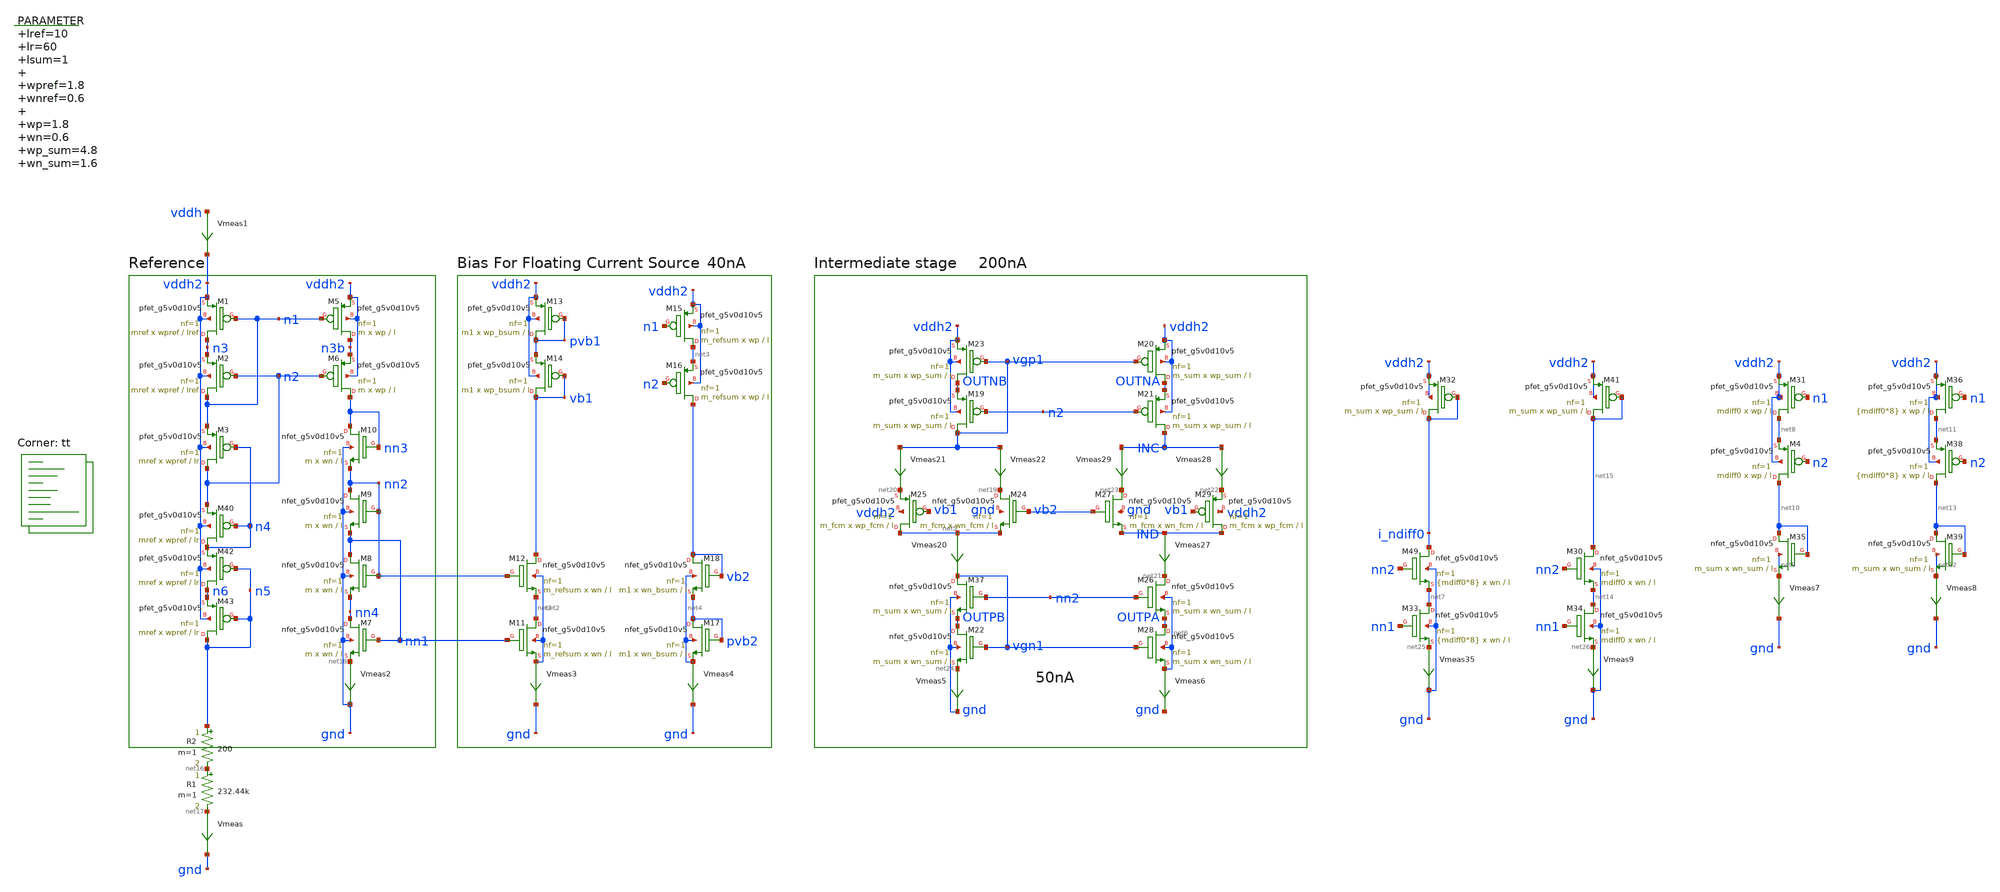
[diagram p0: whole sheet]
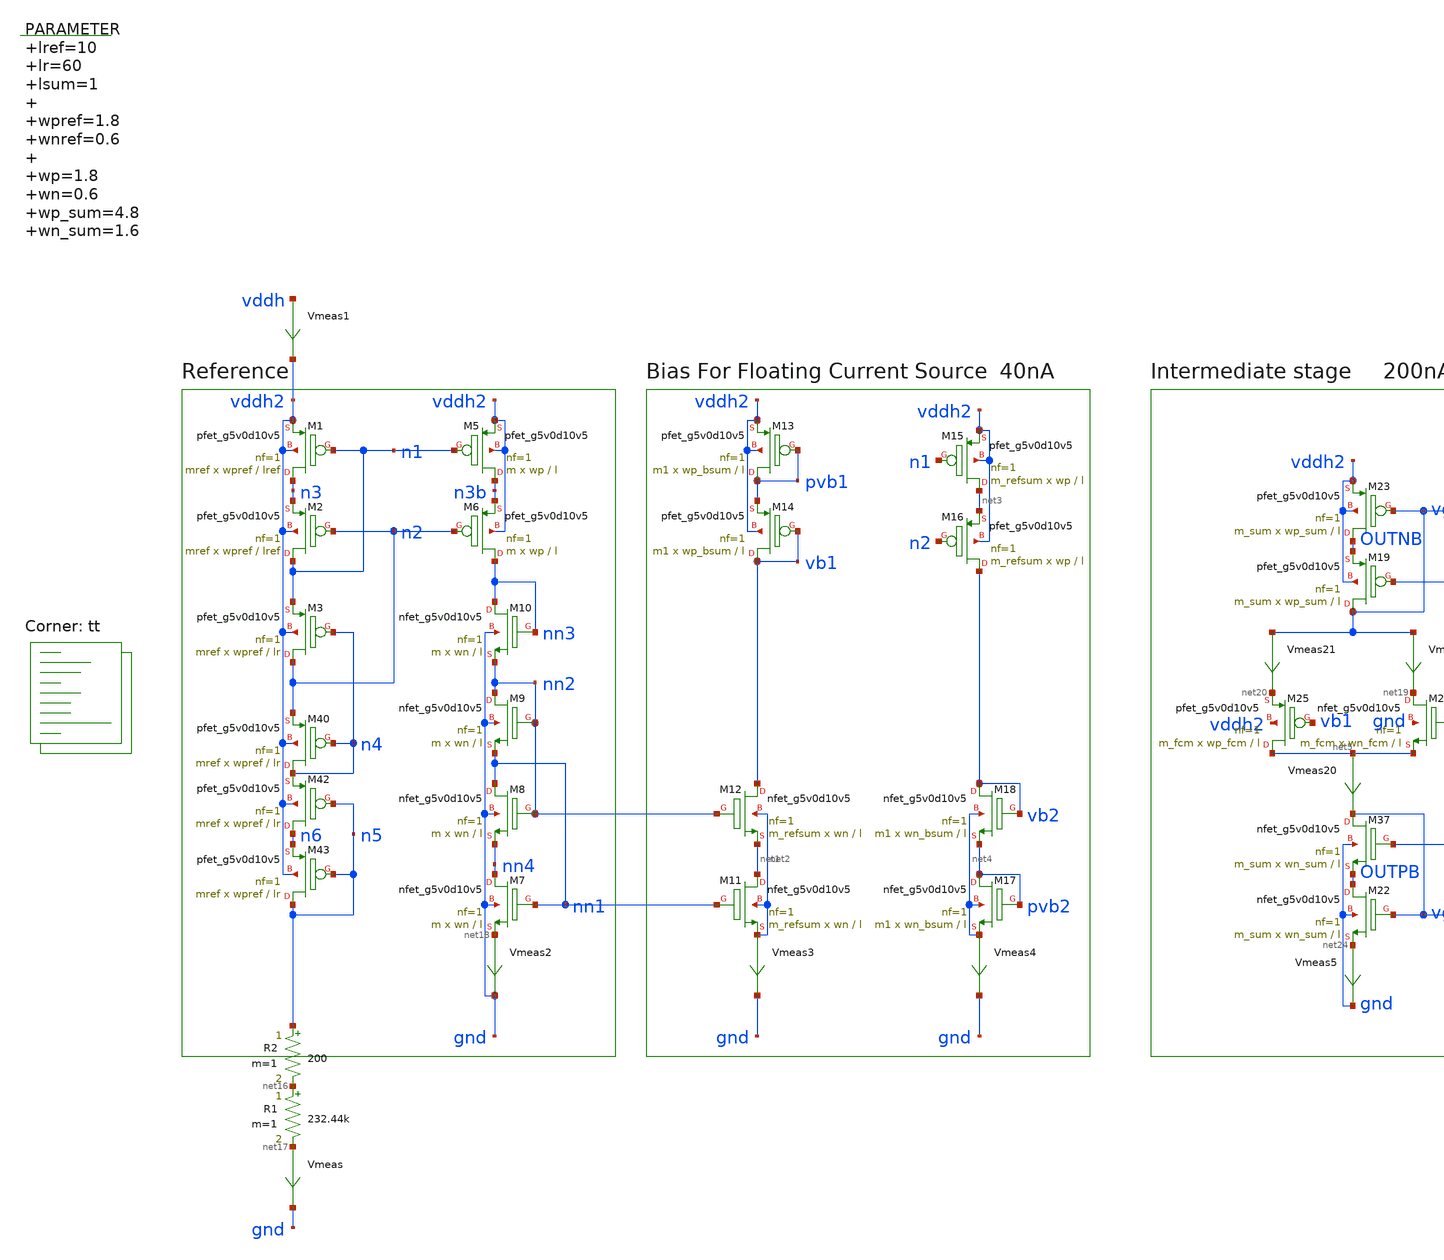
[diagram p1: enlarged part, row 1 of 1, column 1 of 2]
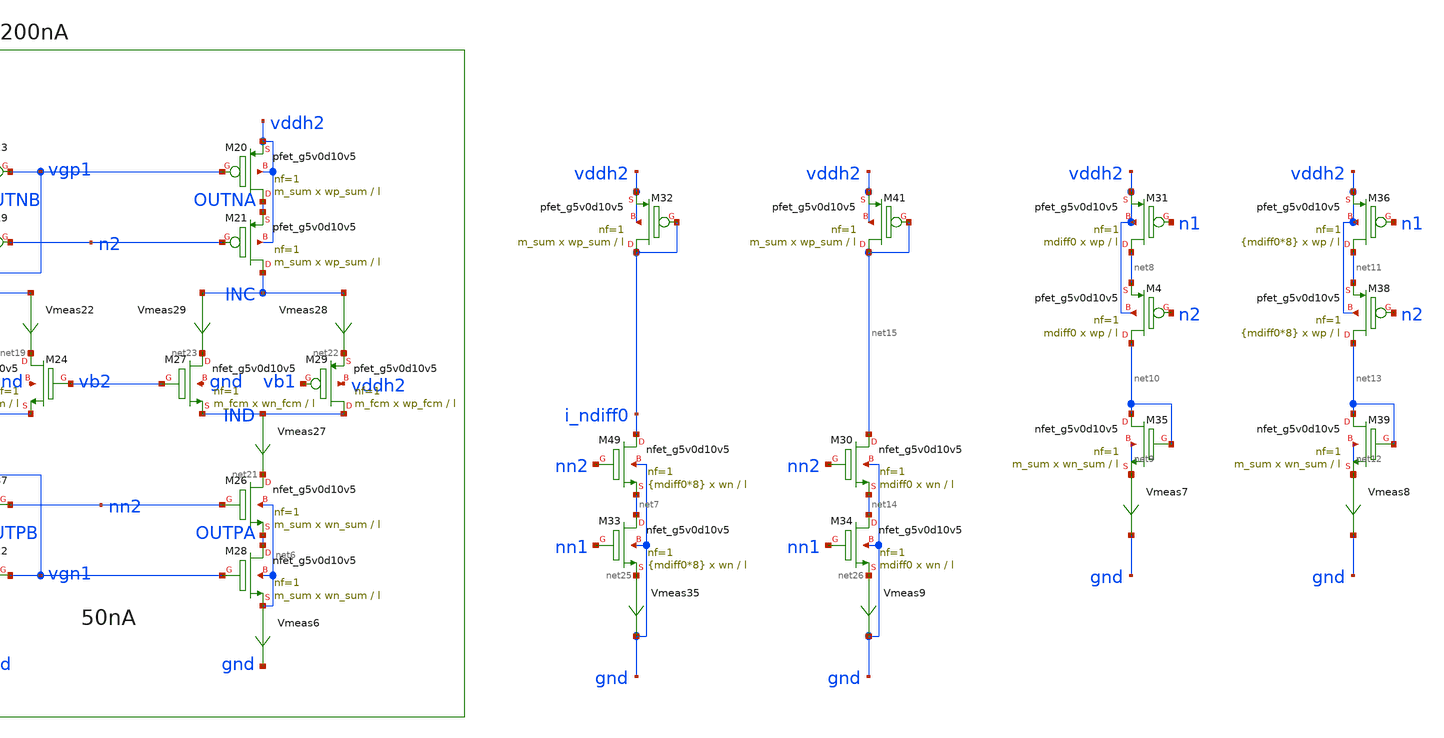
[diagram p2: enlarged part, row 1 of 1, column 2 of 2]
** sch_path: xschem/op_amp_biasing.sch
**.subckt op_amp_biasing
.param lref=10 lr=60 lsum=1 wpref=1.8 wnref=0.6 wp=1.8 wn=0.6 wp_sum=4.8 wn_sum=1.6 wp_fcm=4.8
+ wn_fcm=1.6 wp_head=3 wn_tail=1 wp_bsum=4.8 wn_bsum=1.6 mref=8 m1=2 m_sum=2 m_refsum=5 m_fcm=2 mdiff0=2
XM1 n3 n1 vddh2 vddh2 sky130_fd_pr__pfet_g5v0d10v5 L=lref W=wpref nf=1 ad='int((nf+1)/2) * W/nf * 0.29'
+ as='int((nf+2)/2) * W/nf * 0.29' pd='2*int((nf+1)/2) * (W/nf + 0.29)' ps='2*int((nf+2)/2) * (W/nf + 0.29)'
+ nrd='0.29 / W' nrs='0.29 / W' sa=0 sb=0 sd=0 mult=mref m=mref
R1 net16 net17 232.44k m=1
Vmeas net17 gnd 0
.save i(vmeas)
R2 n5 net16 200 m=1
Vmeas1 vddh vddh2 0
.save i(vmeas1)
XM7 nn4 nn1 net18 gnd sky130_fd_pr__nfet_g5v0d10v5 L=l W=wn nf=1 ad='int((nf+1)/2) * W/nf * 0.29' as='int((nf+2)/2) * W/nf * 0.29'
+ pd='2*int((nf+1)/2) * (W/nf + 0.29)' ps='2*int((nf+2)/2) * (W/nf + 0.29)' nrd='0.29 / W' nrs='0.29 / W'
+ sa=0 sb=0 sd=0 mult=m m=m
XM8 nn1 nn2 nn4 gnd sky130_fd_pr__nfet_g5v0d10v5 L=l W=wn nf=1 ad='int((nf+1)/2) * W/nf * 0.29' as='int((nf+2)/2) * W/nf * 0.29'
+ pd='2*int((nf+1)/2) * (W/nf + 0.29)' ps='2*int((nf+2)/2) * (W/nf + 0.29)' nrd='0.29 / W' nrs='0.29 / W'
+ sa=0 sb=0 sd=0 mult=m m=m
XM9 nn2 nn2 nn1 gnd sky130_fd_pr__nfet_g5v0d10v5 L=l W=wn nf=1 ad='int((nf+1)/2) * W/nf * 0.29' as='int((nf+2)/2) * W/nf * 0.29'
+ pd='2*int((nf+1)/2) * (W/nf + 0.29)' ps='2*int((nf+2)/2) * (W/nf + 0.29)' nrd='0.29 / W' nrs='0.29 / W'
+ sa=0 sb=0 sd=0 mult=m m=m
XM10 nn3 nn3 nn2 gnd sky130_fd_pr__nfet_g5v0d10v5 L=l W=wn nf=1 ad='int((nf+1)/2) * W/nf * 0.29' as='int((nf+2)/2) * W/nf * 0.29'
+ pd='2*int((nf+1)/2) * (W/nf + 0.29)' ps='2*int((nf+2)/2) * (W/nf + 0.29)' nrd='0.29 / W' nrs='0.29 / W'
+ sa=0 sb=0 sd=0 mult=m m=m
Vmeas2 net18 gnd 0
.save i(vmeas2)
XM5 n3b n1 vddh2 vddh2 sky130_fd_pr__pfet_g5v0d10v5 L=l W=wp nf=1 ad='int((nf+1)/2) * W/nf * 0.29' as='int((nf+2)/2) * W/nf * 0.29'
+ pd='2*int((nf+1)/2) * (W/nf + 0.29)' ps='2*int((nf+2)/2) * (W/nf + 0.29)' nrd='0.29 / W' nrs='0.29 / W'
+ sa=0 sb=0 sd=0 mult=m m=m
XM6 nn3 n2 n3b vddh2 sky130_fd_pr__pfet_g5v0d10v5 L=l W=wp nf=1 ad='int((nf+1)/2) * W/nf * 0.29' as='int((nf+2)/2) * W/nf * 0.29'
+ pd='2*int((nf+1)/2) * (W/nf + 0.29)' ps='2*int((nf+2)/2) * (W/nf + 0.29)' nrd='0.29 / W' nrs='0.29 / W'
+ sa=0 sb=0 sd=0 mult=m m=m
XM11 net1 nn1 net2 net2 sky130_fd_pr__nfet_g5v0d10v5 L=l W=wn nf=1 ad='int((nf+1)/2) * W/nf * 0.29' as='int((nf+2)/2) * W/nf * 0.29'
+ pd='2*int((nf+1)/2) * (W/nf + 0.29)' ps='2*int((nf+2)/2) * (W/nf + 0.29)' nrd='0.29 / W' nrs='0.29 / W'
+ sa=0 sb=0 sd=0 mult=m_refsum m=m_refsum
Vmeas3 net2 gnd 0
.save i(vmeas3)
XM17 pvb2 pvb2 net4 net4 sky130_fd_pr__nfet_g5v0d10v5 L=l W=wn_bsum nf=1 ad='int((nf+1)/2) * W/nf * 0.29'
+ as='int((nf+2)/2) * W/nf * 0.29' pd='2*int((nf+1)/2) * (W/nf + 0.29)' ps='2*int((nf+2)/2) * (W/nf + 0.29)'
+ nrd='0.29 / W' nrs='0.29 / W' sa=0 sb=0 sd=0 mult=m1 m=m1
XM18 vb2 vb2 pvb2 net4 sky130_fd_pr__nfet_g5v0d10v5 L=l W=wn_bsum nf=1 ad='int((nf+1)/2) * W/nf * 0.29'
+ as='int((nf+2)/2) * W/nf * 0.29' pd='2*int((nf+1)/2) * (W/nf + 0.29)' ps='2*int((nf+2)/2) * (W/nf + 0.29)'
+ nrd='0.29 / W' nrs='0.29 / W' sa=0 sb=0 sd=0 mult=m1 m=m1
Vmeas4 net4 gnd 0
.save i(vmeas4)
Vmeas20 net5 vgn1 0
.save i(vmeas20)
XM23 OUTNB vgp1 vddh2 vddh2 sky130_fd_pr__pfet_g5v0d10v5 L=l W=wp_sum nf=1 ad='int((nf+1)/2) * W/nf * 0.29'
+ as='int((nf+2)/2) * W/nf * 0.29' pd='2*int((nf+1)/2) * (W/nf + 0.29)' ps='2*int((nf+2)/2) * (W/nf + 0.29)'
+ nrd='0.29 / W' nrs='0.29 / W' sa=0 sb=0 sd=0 mult=m_sum m=m_sum
XM24 net19 vb2 net5 gnd sky130_fd_pr__nfet_g5v0d10v5 L=l W=wn_fcm nf=1 ad='int((nf+1)/2) * W/nf * 0.29'
+ as='int((nf+2)/2) * W/nf * 0.29' pd='2*int((nf+1)/2) * (W/nf + 0.29)' ps='2*int((nf+2)/2) * (W/nf + 0.29)'
+ nrd='0.29 / W' nrs='0.29 / W' sa=0 sb=0 sd=0 mult=m_fcm m=m_fcm
Vmeas21 vgp1 net20 0
.save i(vmeas21)
Vmeas22 vgp1 net19 0
.save i(vmeas22)
XM25 net5 vb1 net20 vddh2 sky130_fd_pr__pfet_g5v0d10v5 L=l W=wp_fcm nf=1 ad='int((nf+1)/2) * W/nf * 0.29'
+ as='int((nf+2)/2) * W/nf * 0.29' pd='2*int((nf+1)/2) * (W/nf + 0.29)' ps='2*int((nf+2)/2) * (W/nf + 0.29)'
+ nrd='0.29 / W' nrs='0.29 / W' sa=0 sb=0 sd=0 mult=m_fcm m=m_fcm
Vmeas27 IND net21 0
.save i(vmeas27)
Vmeas28 INC net22 0
.save i(vmeas28)
Vmeas29 INC net23 0
.save i(vmeas29)
XM37 vgn1 nn2 OUTPB gnd sky130_fd_pr__nfet_g5v0d10v5 L=l W=wn_sum nf=1 ad='int((nf+1)/2) * W/nf * 0.29'
+ as='int((nf+2)/2) * W/nf * 0.29' pd='2*int((nf+1)/2) * (W/nf + 0.29)' ps='2*int((nf+2)/2) * (W/nf + 0.29)'
+ nrd='0.29 / W' nrs='0.29 / W' sa=0 sb=0 sd=0 mult=m_sum m=m_sum
XM13 pvb1 pvb1 vddh2 vddh2 sky130_fd_pr__pfet_g5v0d10v5 L=l W=wp_bsum nf=1 ad='int((nf+1)/2) * W/nf * 0.29'
+ as='int((nf+2)/2) * W/nf * 0.29' pd='2*int((nf+1)/2) * (W/nf + 0.29)' ps='2*int((nf+2)/2) * (W/nf + 0.29)'
+ nrd='0.29 / W' nrs='0.29 / W' sa=0 sb=0 sd=0 mult=m1 m=m1
XM14 vb1 vb1 pvb1 vddh2 sky130_fd_pr__pfet_g5v0d10v5 L=l W=wp_bsum nf=1 ad='int((nf+1)/2) * W/nf * 0.29'
+ as='int((nf+2)/2) * W/nf * 0.29' pd='2*int((nf+1)/2) * (W/nf + 0.29)' ps='2*int((nf+2)/2) * (W/nf + 0.29)'
+ nrd='0.29 / W' nrs='0.29 / W' sa=0 sb=0 sd=0 mult=m1 m=m1
XM15 net3 n1 vddh2 vddh2 sky130_fd_pr__pfet_g5v0d10v5 L=l W=wp nf=1 ad='int((nf+1)/2) * W/nf * 0.29'
+ as='int((nf+2)/2) * W/nf * 0.29' pd='2*int((nf+1)/2) * (W/nf + 0.29)' ps='2*int((nf+2)/2) * (W/nf + 0.29)'
+ nrd='0.29 / W' nrs='0.29 / W' sa=0 sb=0 sd=0 mult=m_refsum m=m_refsum
Vmeas5 net24 gnd 0
.save i(vmeas5)
Vmeas6 net6 gnd 0
.save i(vmeas6)
XM19 vgp1 n2 OUTNB vddh2 sky130_fd_pr__pfet_g5v0d10v5 L=l W=wp_sum nf=1 ad='int((nf+1)/2) * W/nf * 0.29'
+ as='int((nf+2)/2) * W/nf * 0.29' pd='2*int((nf+1)/2) * (W/nf + 0.29)' ps='2*int((nf+2)/2) * (W/nf + 0.29)'
+ nrd='0.29 / W' nrs='0.29 / W' sa=0 sb=0 sd=0 mult=m_sum m=m_sum
XM20 OUTNA vgp1 vddh2 vddh2 sky130_fd_pr__pfet_g5v0d10v5 L=l W=wp_sum nf=1 ad='int((nf+1)/2) * W/nf * 0.29'
+ as='int((nf+2)/2) * W/nf * 0.29' pd='2*int((nf+1)/2) * (W/nf + 0.29)' ps='2*int((nf+2)/2) * (W/nf + 0.29)'
+ nrd='0.29 / W' nrs='0.29 / W' sa=0 sb=0 sd=0 mult=m_sum m=m_sum
XM21 INC n2 OUTNA vddh2 sky130_fd_pr__pfet_g5v0d10v5 L=l W=wp_sum nf=1 ad='int((nf+1)/2) * W/nf * 0.29'
+ as='int((nf+2)/2) * W/nf * 0.29' pd='2*int((nf+1)/2) * (W/nf + 0.29)' ps='2*int((nf+2)/2) * (W/nf + 0.29)'
+ nrd='0.29 / W' nrs='0.29 / W' sa=0 sb=0 sd=0 mult=m_sum m=m_sum
XM22 OUTPB vgn1 net24 gnd sky130_fd_pr__nfet_g5v0d10v5 L=l W=wn_sum nf=1 ad='int((nf+1)/2) * W/nf * 0.29'
+ as='int((nf+2)/2) * W/nf * 0.29' pd='2*int((nf+1)/2) * (W/nf + 0.29)' ps='2*int((nf+2)/2) * (W/nf + 0.29)'
+ nrd='0.29 / W' nrs='0.29 / W' sa=0 sb=0 sd=0 mult=m_sum m=m_sum
XM26 net21 nn2 OUTPA net6 sky130_fd_pr__nfet_g5v0d10v5 L=l W=wn_sum nf=1 ad='int((nf+1)/2) * W/nf * 0.29'
+ as='int((nf+2)/2) * W/nf * 0.29' pd='2*int((nf+1)/2) * (W/nf + 0.29)' ps='2*int((nf+2)/2) * (W/nf + 0.29)'
+ nrd='0.29 / W' nrs='0.29 / W' sa=0 sb=0 sd=0 mult=m_sum m=m_sum
XM49 i_ndiff0 nn2 net7 gnd sky130_fd_pr__nfet_g5v0d10v5 L=l W=wn nf=1 ad='int((nf+1)/2) * W/nf * 0.29'
+ as='int((nf+2)/2) * W/nf * 0.29' pd='2*int((nf+1)/2) * (W/nf + 0.29)' ps='2*int((nf+2)/2) * (W/nf + 0.29)'
+ nrd='0.29 / W' nrs='0.29 / W' sa=0 sb=0 sd=0 mult={mdiff0*8} m={mdiff0*8}
Vmeas35 net25 gnd 0
.save i(vmeas35)
XM32 i_ndiff0 i_ndiff0 vddh2 vddh2 sky130_fd_pr__pfet_g5v0d10v5 L=l W=wp_sum nf=1 ad='int((nf+1)/2) * W/nf * 0.29'
+ as='int((nf+2)/2) * W/nf * 0.29' pd='2*int((nf+1)/2) * (W/nf + 0.29)' ps='2*int((nf+2)/2) * (W/nf + 0.29)'
+ nrd='0.29 / W' nrs='0.29 / W' sa=0 sb=0 sd=0 mult=m_sum m=m_sum
XM28 OUTPA vgn1 net6 net6 sky130_fd_pr__nfet_g5v0d10v5 L=l W=wn_sum nf=1 ad='int((nf+1)/2) * W/nf * 0.29'
+ as='int((nf+2)/2) * W/nf * 0.29' pd='2*int((nf+1)/2) * (W/nf + 0.29)' ps='2*int((nf+2)/2) * (W/nf + 0.29)'
+ nrd='0.29 / W' nrs='0.29 / W' sa=0 sb=0 sd=0 mult=m_sum m=m_sum
XM31 net8 n1 vddh2 vddh2 sky130_fd_pr__pfet_g5v0d10v5 L=l W=wp nf=1 ad='int((nf+1)/2) * W/nf * 0.29'
+ as='int((nf+2)/2) * W/nf * 0.29' pd='2*int((nf+1)/2) * (W/nf + 0.29)' ps='2*int((nf+2)/2) * (W/nf + 0.29)'
+ nrd='0.29 / W' nrs='0.29 / W' sa=0 sb=0 sd=0 mult=mdiff0 m=mdiff0
XM35 net10 net10 net9 net9 sky130_fd_pr__nfet_g5v0d10v5 L=l W=wn_sum nf=1 ad='int((nf+1)/2) * W/nf * 0.29'
+ as='int((nf+2)/2) * W/nf * 0.29' pd='2*int((nf+1)/2) * (W/nf + 0.29)' ps='2*int((nf+2)/2) * (W/nf + 0.29)'
+ nrd='0.29 / W' nrs='0.29 / W' sa=0 sb=0 sd=0 mult=m_sum m=m_sum
Vmeas7 net9 gnd 0
.save i(vmeas7)
XM33 net7 nn1 net25 gnd sky130_fd_pr__nfet_g5v0d10v5 L=l W=wn nf=1 ad='int((nf+1)/2) * W/nf * 0.29' as='int((nf+2)/2) * W/nf * 0.29'
+ pd='2*int((nf+1)/2) * (W/nf + 0.29)' ps='2*int((nf+2)/2) * (W/nf + 0.29)' nrd='0.29 / W' nrs='0.29 / W'
+ sa=0 sb=0 sd=0 mult={mdiff0*8} m={mdiff0*8}
XM36 net11 n1 vddh2 vddh2 sky130_fd_pr__pfet_g5v0d10v5 L=l W=wp nf=1 ad='int((nf+1)/2) * W/nf * 0.29'
+ as='int((nf+2)/2) * W/nf * 0.29' pd='2*int((nf+1)/2) * (W/nf + 0.29)' ps='2*int((nf+2)/2) * (W/nf + 0.29)'
+ nrd='0.29 / W' nrs='0.29 / W' sa=0 sb=0 sd=0 mult={mdiff0*8} m={mdiff0*8}
XM38 net13 n2 net11 vddh2 sky130_fd_pr__pfet_g5v0d10v5 L=l W=wp nf=1 ad='int((nf+1)/2) * W/nf * 0.29'
+ as='int((nf+2)/2) * W/nf * 0.29' pd='2*int((nf+1)/2) * (W/nf + 0.29)' ps='2*int((nf+2)/2) * (W/nf + 0.29)'
+ nrd='0.29 / W' nrs='0.29 / W' sa=0 sb=0 sd=0 mult={mdiff0*8} m={mdiff0*8}
XM39 net13 net13 net12 net12 sky130_fd_pr__nfet_g5v0d10v5 L=l W=wn_sum nf=1 ad='int((nf+1)/2) * W/nf * 0.29'
+ as='int((nf+2)/2) * W/nf * 0.29' pd='2*int((nf+1)/2) * (W/nf + 0.29)' ps='2*int((nf+2)/2) * (W/nf + 0.29)'
+ nrd='0.29 / W' nrs='0.29 / W' sa=0 sb=0 sd=0 mult=m_sum m=m_sum
Vmeas8 net12 gnd 0
.save i(vmeas8)
Vmeas9 net26 gnd 0
.save i(vmeas9)
XM41 net15 net15 vddh2 vddh2 sky130_fd_pr__pfet_g5v0d10v5 L=l W=wp_sum nf=1 ad='int((nf+1)/2) * W/nf * 0.29'
+ as='int((nf+2)/2) * W/nf * 0.29' pd='2*int((nf+1)/2) * (W/nf + 0.29)' ps='2*int((nf+2)/2) * (W/nf + 0.29)'
+ nrd='0.29 / W' nrs='0.29 / W' sa=0 sb=0 sd=0 mult=m_sum m=m_sum
XM12 vb1 nn2 net1 net2 sky130_fd_pr__nfet_g5v0d10v5 L=l W=wn nf=1 ad='int((nf+1)/2) * W/nf * 0.29' as='int((nf+2)/2) * W/nf * 0.29'
+ pd='2*int((nf+1)/2) * (W/nf + 0.29)' ps='2*int((nf+2)/2) * (W/nf + 0.29)' nrd='0.29 / W' nrs='0.29 / W'
+ sa=0 sb=0 sd=0 mult=m_refsum m=m_refsum
XM16 vb2 n2 net3 vddh2 sky130_fd_pr__pfet_g5v0d10v5 L=l W=wp nf=1 ad='int((nf+1)/2) * W/nf * 0.29' as='int((nf+2)/2) * W/nf * 0.29'
+ pd='2*int((nf+1)/2) * (W/nf + 0.29)' ps='2*int((nf+2)/2) * (W/nf + 0.29)' nrd='0.29 / W' nrs='0.29 / W'
+ sa=0 sb=0 sd=0 mult=m_refsum m=m_refsum
XM30 net15 nn2 net14 gnd sky130_fd_pr__nfet_g5v0d10v5 L=l W=wn nf=1 ad='int((nf+1)/2) * W/nf * 0.29'
+ as='int((nf+2)/2) * W/nf * 0.29' pd='2*int((nf+1)/2) * (W/nf + 0.29)' ps='2*int((nf+2)/2) * (W/nf + 0.29)'
+ nrd='0.29 / W' nrs='0.29 / W' sa=0 sb=0 sd=0 mult=mdiff0 m=mdiff0
XM34 net14 nn1 net26 gnd sky130_fd_pr__nfet_g5v0d10v5 L=l W=wn nf=1 ad='int((nf+1)/2) * W/nf * 0.29'
+ as='int((nf+2)/2) * W/nf * 0.29' pd='2*int((nf+1)/2) * (W/nf + 0.29)' ps='2*int((nf+2)/2) * (W/nf + 0.29)'
+ nrd='0.29 / W' nrs='0.29 / W' sa=0 sb=0 sd=0 mult=mdiff0 m=mdiff0
XM4 net10 n2 net8 vddh2 sky130_fd_pr__pfet_g5v0d10v5 L=l W=wp nf=1 ad='int((nf+1)/2) * W/nf * 0.29' as='int((nf+2)/2) * W/nf * 0.29'
+ pd='2*int((nf+1)/2) * (W/nf + 0.29)' ps='2*int((nf+2)/2) * (W/nf + 0.29)' nrd='0.29 / W' nrs='0.29 / W'
+ sa=0 sb=0 sd=0 mult=mdiff0 m=mdiff0
XM29 IND vb1 net22 vddh2 sky130_fd_pr__pfet_g5v0d10v5 L=l W=wp_fcm nf=1 ad='int((nf+1)/2) * W/nf * 0.29'
+ as='int((nf+2)/2) * W/nf * 0.29' pd='2*int((nf+1)/2) * (W/nf + 0.29)' ps='2*int((nf+2)/2) * (W/nf + 0.29)'
+ nrd='0.29 / W' nrs='0.29 / W' sa=0 sb=0 sd=0 mult=m_fcm m=m_fcm
XM27 net23 vb2 IND gnd sky130_fd_pr__nfet_g5v0d10v5 L=l W=wn_fcm nf=1 ad='int((nf+1)/2) * W/nf * 0.29'
+ as='int((nf+2)/2) * W/nf * 0.29' pd='2*int((nf+1)/2) * (W/nf + 0.29)' ps='2*int((nf+2)/2) * (W/nf + 0.29)'
+ nrd='0.29 / W' nrs='0.29 / W' sa=0 sb=0 sd=0 mult=m_fcm m=m_fcm
XM2 n1 n2 n3 vddh2 sky130_fd_pr__pfet_g5v0d10v5 L=lref W=wpref nf=1 ad='int((nf+1)/2) * W/nf * 0.29'
+ as='int((nf+2)/2) * W/nf * 0.29' pd='2*int((nf+1)/2) * (W/nf + 0.29)' ps='2*int((nf+2)/2) * (W/nf + 0.29)'
+ nrd='0.29 / W' nrs='0.29 / W' sa=0 sb=0 sd=0 mult=mref m=mref
XM3 n2 n4 n1 vddh2 sky130_fd_pr__pfet_g5v0d10v5 L=lr W=wpref nf=1 ad='int((nf+1)/2) * W/nf * 0.29' as='int((nf+2)/2) * W/nf * 0.29'
+ pd='2*int((nf+1)/2) * (W/nf + 0.29)' ps='2*int((nf+2)/2) * (W/nf + 0.29)' nrd='0.29 / W' nrs='0.29 / W'
+ sa=0 sb=0 sd=0 mult=mref m=mref
XM40 n4 n4 n2 vddh2 sky130_fd_pr__pfet_g5v0d10v5 L=lr W=wpref nf=1 ad='int((nf+1)/2) * W/nf * 0.29' as='int((nf+2)/2) * W/nf * 0.29'
+ pd='2*int((nf+1)/2) * (W/nf + 0.29)' ps='2*int((nf+2)/2) * (W/nf + 0.29)' nrd='0.29 / W' nrs='0.29 / W'
+ sa=0 sb=0 sd=0 mult=mref m=mref
XM42 n6 n5 n4 vddh2 sky130_fd_pr__pfet_g5v0d10v5 L=lr W=wpref nf=1 ad='int((nf+1)/2) * W/nf * 0.29' as='int((nf+2)/2) * W/nf * 0.29'
+ pd='2*int((nf+1)/2) * (W/nf + 0.29)' ps='2*int((nf+2)/2) * (W/nf + 0.29)' nrd='0.29 / W' nrs='0.29 / W'
+ sa=0 sb=0 sd=0 mult=mref m=mref
XM43 n5 n5 n6 vddh2 sky130_fd_pr__pfet_g5v0d10v5 L=lr W=wpref nf=1 ad='int((nf+1)/2) * W/nf * 0.29' as='int((nf+2)/2) * W/nf * 0.29'
+ pd='2*int((nf+1)/2) * (W/nf + 0.29)' ps='2*int((nf+2)/2) * (W/nf + 0.29)' nrd='0.29 / W' nrs='0.29 / W'
+ sa=0 sb=0 sd=0 mult=mref m=mref
**** begin user architecture code
.lib $::SKYWATER_MODELS/sky130.lib.spice tt



  .option wnflag=1
  .option safecurrents
  ********************Static Current Sources***************************
  .param iref=10u
  *Iref n4 gnd 100n
  ********************Static Voltage Sources***************************
  Vddh vddh gnd dc 5.5
  ********************Simulation Commands*****************************
  .control
     reset
     save all
     *tran 1n 10u
     dc R1 1meg 1.2meg 1k
     write biasing-tb.raw
     set appendwrite
*    quit 0
  .endc



**** end user architecture code
**.ends
.end
